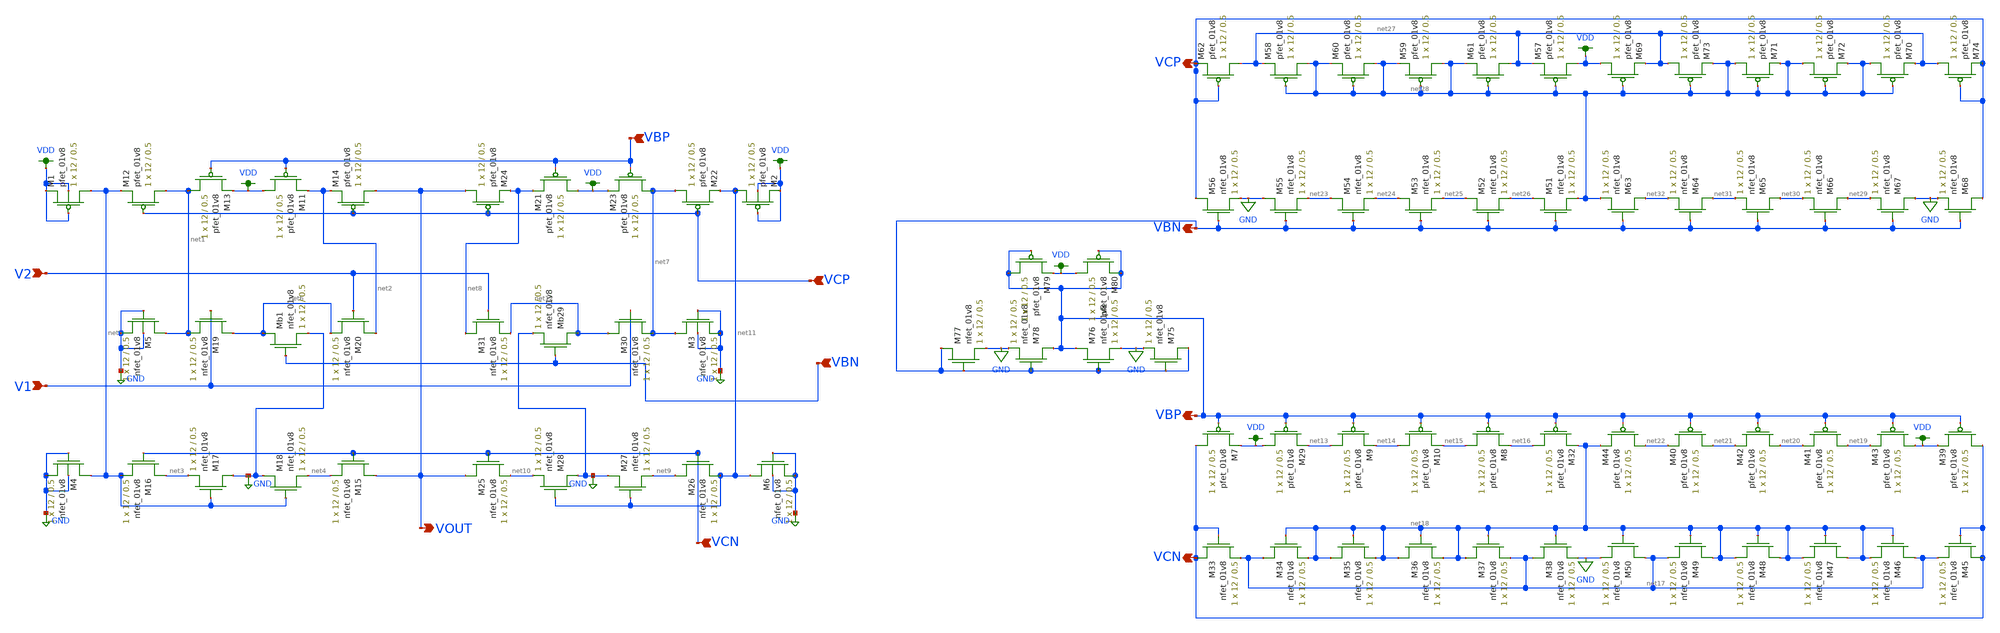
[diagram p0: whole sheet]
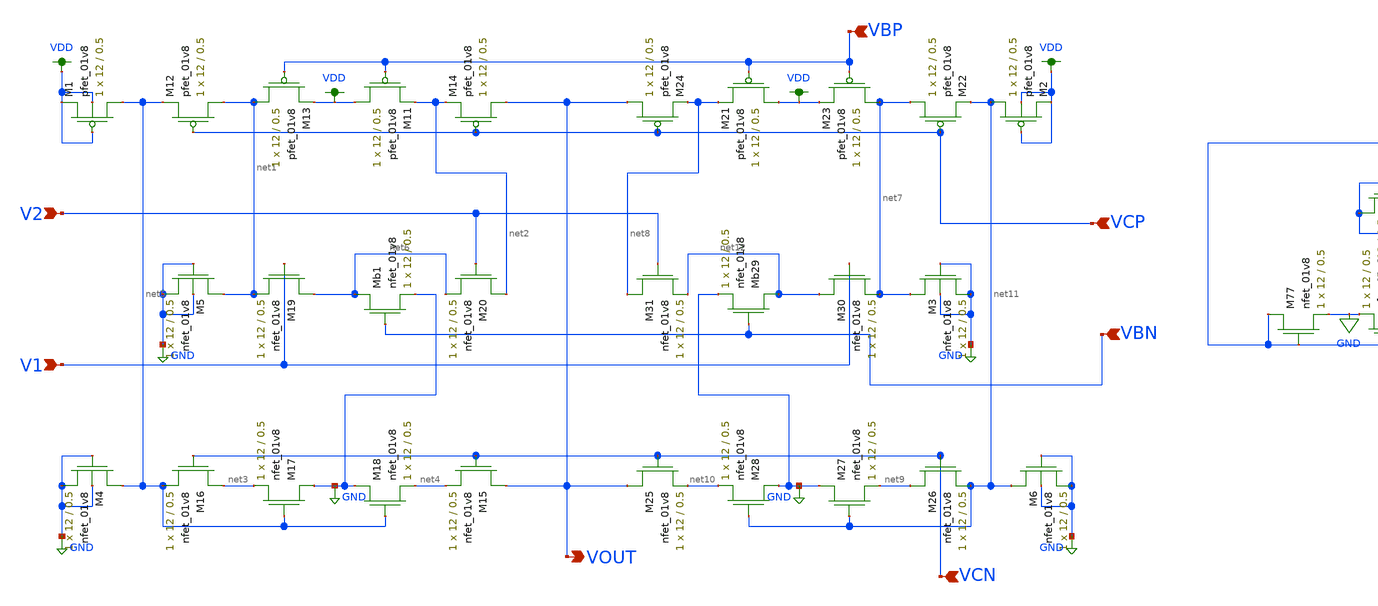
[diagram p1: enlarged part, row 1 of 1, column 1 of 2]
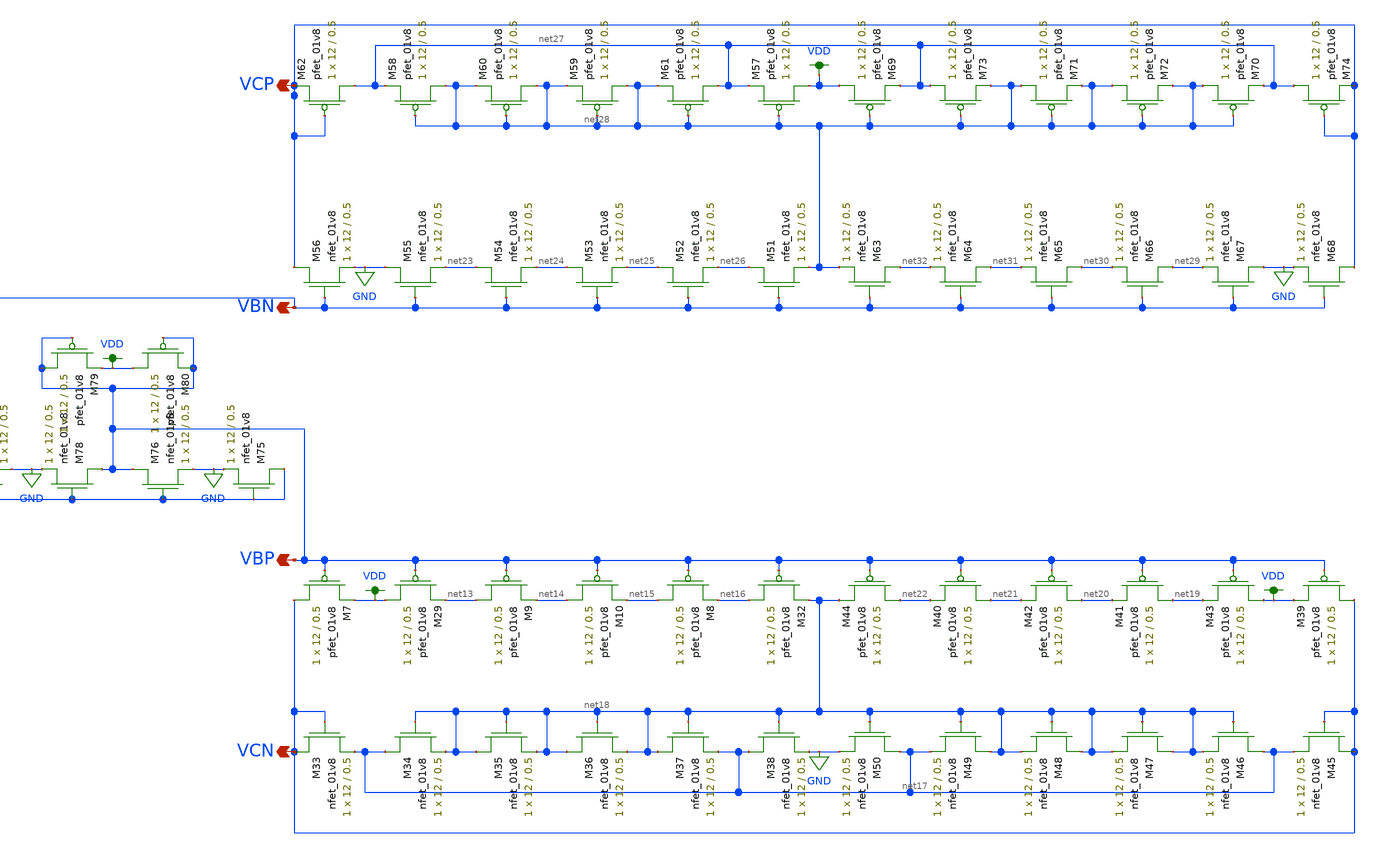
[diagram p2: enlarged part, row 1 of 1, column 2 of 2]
** sch_path: MP3/LVS/LVS_Circuit.sch
**.subckt LVS_Circuit VBP VCN VCP VOUT VBN V2 V1 VBP VCN VCP VBN
*.ipin VBP
*.ipin VCN
*.ipin VCP
*.opin VOUT
*.ipin VBN
*.ipin V2
*.ipin V1
*.opin VBP
*.opin VCN
*.opin VCP
*.opin VBN
XM11 VDD VBP net2 VDD sky130_fd_pr__pfet_01v8 L=0.5 W=12 nf=1 ad='int((nf+1)/2) * W/nf * 0.29' as='int((nf+2)/2) * W/nf * 0.29'
+ pd='2*int((nf+1)/2) * (W/nf + 0.29)' ps='2*int((nf+2)/2) * (W/nf + 0.29)' nrd='0.29 / W' nrs='0.29 / W'
+ sa=0 sb=0 sd=0 mult=1 m=1
XM12 net1 VCP net5 VDD sky130_fd_pr__pfet_01v8 L=0.5 W=12 nf=1 ad='int((nf+1)/2) * W/nf * 0.29' as='int((nf+2)/2) * W/nf * 0.29'
+ pd='2*int((nf+1)/2) * (W/nf + 0.29)' ps='2*int((nf+2)/2) * (W/nf + 0.29)' nrd='0.29 / W' nrs='0.29 / W'
+ sa=0 sb=0 sd=0 mult=1 m=1
XM13 net1 VBP VDD VDD sky130_fd_pr__pfet_01v8 L=0.5 W=12 nf=1 ad='int((nf+1)/2) * W/nf * 0.29' as='int((nf+2)/2) * W/nf * 0.29'
+ pd='2*int((nf+1)/2) * (W/nf + 0.29)' ps='2*int((nf+2)/2) * (W/nf + 0.29)' nrd='0.29 / W' nrs='0.29 / W'
+ sa=0 sb=0 sd=0 mult=1 m=1
XM14 VOUT VCP net2 VDD sky130_fd_pr__pfet_01v8 L=0.5 W=12 nf=1 ad='int((nf+1)/2) * W/nf * 0.29' as='int((nf+2)/2) * W/nf * 0.29'
+ pd='2*int((nf+1)/2) * (W/nf + 0.29)' ps='2*int((nf+2)/2) * (W/nf + 0.29)' nrd='0.29 / W' nrs='0.29 / W'
+ sa=0 sb=0 sd=0 mult=1 m=1
XM15 VOUT VCN net4 GND sky130_fd_pr__nfet_01v8 L=0.5 W=12 nf=1 ad='int((nf+1)/2) * W/nf * 0.29' as='int((nf+2)/2) * W/nf * 0.29'
+ pd='2*int((nf+1)/2) * (W/nf + 0.29)' ps='2*int((nf+2)/2) * (W/nf + 0.29)' nrd='0.29 / W' nrs='0.29 / W'
+ sa=0 sb=0 sd=0 mult=1 m=1
XM16 net3 VCN net5 GND sky130_fd_pr__nfet_01v8 L=0.5 W=12 nf=1 ad='int((nf+1)/2) * W/nf * 0.29' as='int((nf+2)/2) * W/nf * 0.29'
+ pd='2*int((nf+1)/2) * (W/nf + 0.29)' ps='2*int((nf+2)/2) * (W/nf + 0.29)' nrd='0.29 / W' nrs='0.29 / W'
+ sa=0 sb=0 sd=0 mult=1 m=1
XM17 GND net5 net3 GND sky130_fd_pr__nfet_01v8 L=0.5 W=12 nf=1 ad='int((nf+1)/2) * W/nf * 0.29' as='int((nf+2)/2) * W/nf * 0.29'
+ pd='2*int((nf+1)/2) * (W/nf + 0.29)' ps='2*int((nf+2)/2) * (W/nf + 0.29)' nrd='0.29 / W' nrs='0.29 / W'
+ sa=0 sb=0 sd=0 mult=1 m=1
XM18 GND net5 net4 GND sky130_fd_pr__nfet_01v8 L=0.5 W=12 nf=1 ad='int((nf+1)/2) * W/nf * 0.29' as='int((nf+2)/2) * W/nf * 0.29'
+ pd='2*int((nf+1)/2) * (W/nf + 0.29)' ps='2*int((nf+2)/2) * (W/nf + 0.29)' nrd='0.29 / W' nrs='0.29 / W'
+ sa=0 sb=0 sd=0 mult=1 m=1
XMb1 net6 VBN GND GND sky130_fd_pr__nfet_01v8 L=0.5 W=12 nf=1 ad='int((nf+1)/2) * W/nf * 0.29' as='int((nf+2)/2) * W/nf * 0.29'
+ pd='2*int((nf+1)/2) * (W/nf + 0.29)' ps='2*int((nf+2)/2) * (W/nf + 0.29)' nrd='0.29 / W' nrs='0.29 / W'
+ sa=0 sb=0 sd=0 mult=1 m=1
XM19 net6 V1 net1 GND sky130_fd_pr__nfet_01v8 L=0.5 W=12 nf=1 ad='int((nf+1)/2) * W/nf * 0.29' as='int((nf+2)/2) * W/nf * 0.29'
+ pd='2*int((nf+1)/2) * (W/nf + 0.29)' ps='2*int((nf+2)/2) * (W/nf + 0.29)' nrd='0.29 / W' nrs='0.29 / W'
+ sa=0 sb=0 sd=0 mult=1 m=1
XM20 net2 V2 net6 GND sky130_fd_pr__nfet_01v8 L=0.5 W=12 nf=1 ad='int((nf+1)/2) * W/nf * 0.29' as='int((nf+2)/2) * W/nf * 0.29'
+ pd='2*int((nf+1)/2) * (W/nf + 0.29)' ps='2*int((nf+2)/2) * (W/nf + 0.29)' nrd='0.29 / W' nrs='0.29 / W'
+ sa=0 sb=0 sd=0 mult=1 m=1
XM21 VDD VBP net8 VDD sky130_fd_pr__pfet_01v8 L=0.5 W=12 nf=1 ad='int((nf+1)/2) * W/nf * 0.29' as='int((nf+2)/2) * W/nf * 0.29'
+ pd='2*int((nf+1)/2) * (W/nf + 0.29)' ps='2*int((nf+2)/2) * (W/nf + 0.29)' nrd='0.29 / W' nrs='0.29 / W'
+ sa=0 sb=0 sd=0 mult=1 m=1
XM22 net7 VCP net11 VDD sky130_fd_pr__pfet_01v8 L=0.5 W=12 nf=1 ad='int((nf+1)/2) * W/nf * 0.29' as='int((nf+2)/2) * W/nf * 0.29'
+ pd='2*int((nf+1)/2) * (W/nf + 0.29)' ps='2*int((nf+2)/2) * (W/nf + 0.29)' nrd='0.29 / W' nrs='0.29 / W'
+ sa=0 sb=0 sd=0 mult=1 m=1
XM23 net7 VBP VDD VDD sky130_fd_pr__pfet_01v8 L=0.5 W=12 nf=1 ad='int((nf+1)/2) * W/nf * 0.29' as='int((nf+2)/2) * W/nf * 0.29'
+ pd='2*int((nf+1)/2) * (W/nf + 0.29)' ps='2*int((nf+2)/2) * (W/nf + 0.29)' nrd='0.29 / W' nrs='0.29 / W'
+ sa=0 sb=0 sd=0 mult=1 m=1
XM24 VOUT VCP net8 VDD sky130_fd_pr__pfet_01v8 L=0.5 W=12 nf=1 ad='int((nf+1)/2) * W/nf * 0.29' as='int((nf+2)/2) * W/nf * 0.29'
+ pd='2*int((nf+1)/2) * (W/nf + 0.29)' ps='2*int((nf+2)/2) * (W/nf + 0.29)' nrd='0.29 / W' nrs='0.29 / W'
+ sa=0 sb=0 sd=0 mult=1 m=1
XM25 VOUT VCN net10 GND sky130_fd_pr__nfet_01v8 L=0.5 W=12 nf=1 ad='int((nf+1)/2) * W/nf * 0.29' as='int((nf+2)/2) * W/nf * 0.29'
+ pd='2*int((nf+1)/2) * (W/nf + 0.29)' ps='2*int((nf+2)/2) * (W/nf + 0.29)' nrd='0.29 / W' nrs='0.29 / W'
+ sa=0 sb=0 sd=0 mult=1 m=1
XM26 net9 VCN net11 GND sky130_fd_pr__nfet_01v8 L=0.5 W=12 nf=1 ad='int((nf+1)/2) * W/nf * 0.29' as='int((nf+2)/2) * W/nf * 0.29'
+ pd='2*int((nf+1)/2) * (W/nf + 0.29)' ps='2*int((nf+2)/2) * (W/nf + 0.29)' nrd='0.29 / W' nrs='0.29 / W'
+ sa=0 sb=0 sd=0 mult=1 m=1
XM27 GND net11 net9 GND sky130_fd_pr__nfet_01v8 L=0.5 W=12 nf=1 ad='int((nf+1)/2) * W/nf * 0.29' as='int((nf+2)/2) * W/nf * 0.29'
+ pd='2*int((nf+1)/2) * (W/nf + 0.29)' ps='2*int((nf+2)/2) * (W/nf + 0.29)' nrd='0.29 / W' nrs='0.29 / W'
+ sa=0 sb=0 sd=0 mult=1 m=1
XM28 GND net11 net10 GND sky130_fd_pr__nfet_01v8 L=0.5 W=12 nf=1 ad='int((nf+1)/2) * W/nf * 0.29' as='int((nf+2)/2) * W/nf * 0.29'
+ pd='2*int((nf+1)/2) * (W/nf + 0.29)' ps='2*int((nf+2)/2) * (W/nf + 0.29)' nrd='0.29 / W' nrs='0.29 / W'
+ sa=0 sb=0 sd=0 mult=1 m=1
XMb29 net12 VBN GND GND sky130_fd_pr__nfet_01v8 L=0.5 W=12 nf=1 ad='int((nf+1)/2) * W/nf * 0.29' as='int((nf+2)/2) * W/nf * 0.29'
+ pd='2*int((nf+1)/2) * (W/nf + 0.29)' ps='2*int((nf+2)/2) * (W/nf + 0.29)' nrd='0.29 / W' nrs='0.29 / W'
+ sa=0 sb=0 sd=0 mult=1 m=1
XM30 net12 V1 net7 GND sky130_fd_pr__nfet_01v8 L=0.5 W=12 nf=1 ad='int((nf+1)/2) * W/nf * 0.29' as='int((nf+2)/2) * W/nf * 0.29'
+ pd='2*int((nf+1)/2) * (W/nf + 0.29)' ps='2*int((nf+2)/2) * (W/nf + 0.29)' nrd='0.29 / W' nrs='0.29 / W'
+ sa=0 sb=0 sd=0 mult=1 m=1
XM31 net8 V2 net12 GND sky130_fd_pr__nfet_01v8 L=0.5 W=12 nf=1 ad='int((nf+1)/2) * W/nf * 0.29' as='int((nf+2)/2) * W/nf * 0.29'
+ pd='2*int((nf+1)/2) * (W/nf + 0.29)' ps='2*int((nf+2)/2) * (W/nf + 0.29)' nrd='0.29 / W' nrs='0.29 / W'
+ sa=0 sb=0 sd=0 mult=1 m=1
XM1 net5 VDD VDD VDD sky130_fd_pr__pfet_01v8 L=0.5 W=12 nf=1 ad='int((nf+1)/2) * W/nf * 0.29' as='int((nf+2)/2) * W/nf * 0.29'
+ pd='2*int((nf+1)/2) * (W/nf + 0.29)' ps='2*int((nf+2)/2) * (W/nf + 0.29)' nrd='0.29 / W' nrs='0.29 / W'
+ sa=0 sb=0 sd=0 mult=1 m=1
XM2 net11 VDD VDD VDD sky130_fd_pr__pfet_01v8 L=0.5 W=12 nf=1 ad='int((nf+1)/2) * W/nf * 0.29' as='int((nf+2)/2) * W/nf * 0.29'
+ pd='2*int((nf+1)/2) * (W/nf + 0.29)' ps='2*int((nf+2)/2) * (W/nf + 0.29)' nrd='0.29 / W' nrs='0.29 / W'
+ sa=0 sb=0 sd=0 mult=1 m=1
XM4 net5 GND GND GND sky130_fd_pr__nfet_01v8 L=0.5 W=12 nf=1 ad='int((nf+1)/2) * W/nf * 0.29' as='int((nf+2)/2) * W/nf * 0.29'
+ pd='2*int((nf+1)/2) * (W/nf + 0.29)' ps='2*int((nf+2)/2) * (W/nf + 0.29)' nrd='0.29 / W' nrs='0.29 / W'
+ sa=0 sb=0 sd=0 mult=1 m=1
XM3 net7 GND GND GND sky130_fd_pr__nfet_01v8 L=0.5 W=12 nf=1 ad='int((nf+1)/2) * W/nf * 0.29' as='int((nf+2)/2) * W/nf * 0.29'
+ pd='2*int((nf+1)/2) * (W/nf + 0.29)' ps='2*int((nf+2)/2) * (W/nf + 0.29)' nrd='0.29 / W' nrs='0.29 / W'
+ sa=0 sb=0 sd=0 mult=1 m=1
XM5 net1 GND GND GND sky130_fd_pr__nfet_01v8 L=0.5 W=12 nf=1 ad='int((nf+1)/2) * W/nf * 0.29' as='int((nf+2)/2) * W/nf * 0.29'
+ pd='2*int((nf+1)/2) * (W/nf + 0.29)' ps='2*int((nf+2)/2) * (W/nf + 0.29)' nrd='0.29 / W' nrs='0.29 / W'
+ sa=0 sb=0 sd=0 mult=1 m=1
XM6 net11 GND GND GND sky130_fd_pr__nfet_01v8 L=0.5 W=12 nf=1 ad='int((nf+1)/2) * W/nf * 0.29' as='int((nf+2)/2) * W/nf * 0.29'
+ pd='2*int((nf+1)/2) * (W/nf + 0.29)' ps='2*int((nf+2)/2) * (W/nf + 0.29)' nrd='0.29 / W' nrs='0.29 / W'
+ sa=0 sb=0 sd=0 mult=1 m=1
XM7 VCN VBP VDD VDD sky130_fd_pr__pfet_01v8 L=0.5 W=12 nf=1 ad='int((nf+1)/2) * W/nf * 0.29' as='int((nf+2)/2) * W/nf * 0.29'
+ pd='2*int((nf+1)/2) * (W/nf + 0.29)' ps='2*int((nf+2)/2) * (W/nf + 0.29)' nrd='0.29 / W' nrs='0.29 / W'
+ sa=0 sb=0 sd=0 mult=1 m=1
XM8 net15 VBP net16 VDD sky130_fd_pr__pfet_01v8 L=0.5 W=12 nf=1 ad='int((nf+1)/2) * W/nf * 0.29' as='int((nf+2)/2) * W/nf * 0.29'
+ pd='2*int((nf+1)/2) * (W/nf + 0.29)' ps='2*int((nf+2)/2) * (W/nf + 0.29)' nrd='0.29 / W' nrs='0.29 / W'
+ sa=0 sb=0 sd=0 mult=1 m=1
XM9 net13 VBP net14 VDD sky130_fd_pr__pfet_01v8 L=0.5 W=12 nf=1 ad='int((nf+1)/2) * W/nf * 0.29' as='int((nf+2)/2) * W/nf * 0.29'
+ pd='2*int((nf+1)/2) * (W/nf + 0.29)' ps='2*int((nf+2)/2) * (W/nf + 0.29)' nrd='0.29 / W' nrs='0.29 / W'
+ sa=0 sb=0 sd=0 mult=1 m=1
XM10 net14 VBP net15 VDD sky130_fd_pr__pfet_01v8 L=0.5 W=12 nf=1 ad='int((nf+1)/2) * W/nf * 0.29' as='int((nf+2)/2) * W/nf * 0.29'
+ pd='2*int((nf+1)/2) * (W/nf + 0.29)' ps='2*int((nf+2)/2) * (W/nf + 0.29)' nrd='0.29 / W' nrs='0.29 / W'
+ sa=0 sb=0 sd=0 mult=1 m=1
XM29 VDD VBP net13 VDD sky130_fd_pr__pfet_01v8 L=0.5 W=12 nf=1 ad='int((nf+1)/2) * W/nf * 0.29' as='int((nf+2)/2) * W/nf * 0.29'
+ pd='2*int((nf+1)/2) * (W/nf + 0.29)' ps='2*int((nf+2)/2) * (W/nf + 0.29)' nrd='0.29 / W' nrs='0.29 / W'
+ sa=0 sb=0 sd=0 mult=1 m=1
XM32 net16 VBP net18 VDD sky130_fd_pr__pfet_01v8 L=0.5 W=12 nf=1 ad='int((nf+1)/2) * W/nf * 0.29' as='int((nf+2)/2) * W/nf * 0.29'
+ pd='2*int((nf+1)/2) * (W/nf + 0.29)' ps='2*int((nf+2)/2) * (W/nf + 0.29)' nrd='0.29 / W' nrs='0.29 / W'
+ sa=0 sb=0 sd=0 mult=1 m=1
XM33 VCN VCN net17 GND sky130_fd_pr__nfet_01v8 L=0.5 W=12 nf=1 ad='int((nf+1)/2) * W/nf * 0.29' as='int((nf+2)/2) * W/nf * 0.29'
+ pd='2*int((nf+1)/2) * (W/nf + 0.29)' ps='2*int((nf+2)/2) * (W/nf + 0.29)' nrd='0.29 / W' nrs='0.29 / W'
+ sa=0 sb=0 sd=0 mult=1 m=1
XM34 net17 net18 net18 GND sky130_fd_pr__nfet_01v8 L=0.5 W=12 nf=1 ad='int((nf+1)/2) * W/nf * 0.29' as='int((nf+2)/2) * W/nf * 0.29'
+ pd='2*int((nf+1)/2) * (W/nf + 0.29)' ps='2*int((nf+2)/2) * (W/nf + 0.29)' nrd='0.29 / W' nrs='0.29 / W'
+ sa=0 sb=0 sd=0 mult=1 m=1
XM35 net18 net18 net18 GND sky130_fd_pr__nfet_01v8 L=0.5 W=12 nf=1 ad='int((nf+1)/2) * W/nf * 0.29' as='int((nf+2)/2) * W/nf * 0.29'
+ pd='2*int((nf+1)/2) * (W/nf + 0.29)' ps='2*int((nf+2)/2) * (W/nf + 0.29)' nrd='0.29 / W' nrs='0.29 / W'
+ sa=0 sb=0 sd=0 mult=1 m=1
XM36 net18 net18 net18 GND sky130_fd_pr__nfet_01v8 L=0.5 W=12 nf=1 ad='int((nf+1)/2) * W/nf * 0.29' as='int((nf+2)/2) * W/nf * 0.29'
+ pd='2*int((nf+1)/2) * (W/nf + 0.29)' ps='2*int((nf+2)/2) * (W/nf + 0.29)' nrd='0.29 / W' nrs='0.29 / W'
+ sa=0 sb=0 sd=0 mult=1 m=1
XM37 net18 net18 net17 GND sky130_fd_pr__nfet_01v8 L=0.5 W=12 nf=1 ad='int((nf+1)/2) * W/nf * 0.29' as='int((nf+2)/2) * W/nf * 0.29'
+ pd='2*int((nf+1)/2) * (W/nf + 0.29)' ps='2*int((nf+2)/2) * (W/nf + 0.29)' nrd='0.29 / W' nrs='0.29 / W'
+ sa=0 sb=0 sd=0 mult=1 m=1
XM38 net17 net18 GND GND sky130_fd_pr__nfet_01v8 L=0.5 W=12 nf=1 ad='int((nf+1)/2) * W/nf * 0.29' as='int((nf+2)/2) * W/nf * 0.29'
+ pd='2*int((nf+1)/2) * (W/nf + 0.29)' ps='2*int((nf+2)/2) * (W/nf + 0.29)' nrd='0.29 / W' nrs='0.29 / W'
+ sa=0 sb=0 sd=0 mult=1 m=1
XM39 VCN VBP VDD VDD sky130_fd_pr__pfet_01v8 L=0.5 W=12 nf=1 ad='int((nf+1)/2) * W/nf * 0.29' as='int((nf+2)/2) * W/nf * 0.29'
+ pd='2*int((nf+1)/2) * (W/nf + 0.29)' ps='2*int((nf+2)/2) * (W/nf + 0.29)' nrd='0.29 / W' nrs='0.29 / W'
+ sa=0 sb=0 sd=0 mult=1 m=1
XM40 net21 VBP net22 VDD sky130_fd_pr__pfet_01v8 L=0.5 W=12 nf=1 ad='int((nf+1)/2) * W/nf * 0.29' as='int((nf+2)/2) * W/nf * 0.29'
+ pd='2*int((nf+1)/2) * (W/nf + 0.29)' ps='2*int((nf+2)/2) * (W/nf + 0.29)' nrd='0.29 / W' nrs='0.29 / W'
+ sa=0 sb=0 sd=0 mult=1 m=1
XM41 net19 VBP net20 VDD sky130_fd_pr__pfet_01v8 L=0.5 W=12 nf=1 ad='int((nf+1)/2) * W/nf * 0.29' as='int((nf+2)/2) * W/nf * 0.29'
+ pd='2*int((nf+1)/2) * (W/nf + 0.29)' ps='2*int((nf+2)/2) * (W/nf + 0.29)' nrd='0.29 / W' nrs='0.29 / W'
+ sa=0 sb=0 sd=0 mult=1 m=1
XM42 net20 VBP net21 VDD sky130_fd_pr__pfet_01v8 L=0.5 W=12 nf=1 ad='int((nf+1)/2) * W/nf * 0.29' as='int((nf+2)/2) * W/nf * 0.29'
+ pd='2*int((nf+1)/2) * (W/nf + 0.29)' ps='2*int((nf+2)/2) * (W/nf + 0.29)' nrd='0.29 / W' nrs='0.29 / W'
+ sa=0 sb=0 sd=0 mult=1 m=1
XM43 VDD VBP net19 VDD sky130_fd_pr__pfet_01v8 L=0.5 W=12 nf=1 ad='int((nf+1)/2) * W/nf * 0.29' as='int((nf+2)/2) * W/nf * 0.29'
+ pd='2*int((nf+1)/2) * (W/nf + 0.29)' ps='2*int((nf+2)/2) * (W/nf + 0.29)' nrd='0.29 / W' nrs='0.29 / W'
+ sa=0 sb=0 sd=0 mult=1 m=1
XM44 net22 VBP net18 VDD sky130_fd_pr__pfet_01v8 L=0.5 W=12 nf=1 ad='int((nf+1)/2) * W/nf * 0.29' as='int((nf+2)/2) * W/nf * 0.29'
+ pd='2*int((nf+1)/2) * (W/nf + 0.29)' ps='2*int((nf+2)/2) * (W/nf + 0.29)' nrd='0.29 / W' nrs='0.29 / W'
+ sa=0 sb=0 sd=0 mult=1 m=1
XM45 VCN VCN net17 GND sky130_fd_pr__nfet_01v8 L=0.5 W=12 nf=1 ad='int((nf+1)/2) * W/nf * 0.29' as='int((nf+2)/2) * W/nf * 0.29'
+ pd='2*int((nf+1)/2) * (W/nf + 0.29)' ps='2*int((nf+2)/2) * (W/nf + 0.29)' nrd='0.29 / W' nrs='0.29 / W'
+ sa=0 sb=0 sd=0 mult=1 m=1
XM46 net17 net18 net18 GND sky130_fd_pr__nfet_01v8 L=0.5 W=12 nf=1 ad='int((nf+1)/2) * W/nf * 0.29' as='int((nf+2)/2) * W/nf * 0.29'
+ pd='2*int((nf+1)/2) * (W/nf + 0.29)' ps='2*int((nf+2)/2) * (W/nf + 0.29)' nrd='0.29 / W' nrs='0.29 / W'
+ sa=0 sb=0 sd=0 mult=1 m=1
XM47 net18 net18 net18 GND sky130_fd_pr__nfet_01v8 L=0.5 W=12 nf=1 ad='int((nf+1)/2) * W/nf * 0.29' as='int((nf+2)/2) * W/nf * 0.29'
+ pd='2*int((nf+1)/2) * (W/nf + 0.29)' ps='2*int((nf+2)/2) * (W/nf + 0.29)' nrd='0.29 / W' nrs='0.29 / W'
+ sa=0 sb=0 sd=0 mult=1 m=1
XM48 net18 net18 net18 GND sky130_fd_pr__nfet_01v8 L=0.5 W=12 nf=1 ad='int((nf+1)/2) * W/nf * 0.29' as='int((nf+2)/2) * W/nf * 0.29'
+ pd='2*int((nf+1)/2) * (W/nf + 0.29)' ps='2*int((nf+2)/2) * (W/nf + 0.29)' nrd='0.29 / W' nrs='0.29 / W'
+ sa=0 sb=0 sd=0 mult=1 m=1
XM49 net18 net18 net17 GND sky130_fd_pr__nfet_01v8 L=0.5 W=12 nf=1 ad='int((nf+1)/2) * W/nf * 0.29' as='int((nf+2)/2) * W/nf * 0.29'
+ pd='2*int((nf+1)/2) * (W/nf + 0.29)' ps='2*int((nf+2)/2) * (W/nf + 0.29)' nrd='0.29 / W' nrs='0.29 / W'
+ sa=0 sb=0 sd=0 mult=1 m=1
XM50 net17 net18 GND GND sky130_fd_pr__nfet_01v8 L=0.5 W=12 nf=1 ad='int((nf+1)/2) * W/nf * 0.29' as='int((nf+2)/2) * W/nf * 0.29'
+ pd='2*int((nf+1)/2) * (W/nf + 0.29)' ps='2*int((nf+2)/2) * (W/nf + 0.29)' nrd='0.29 / W' nrs='0.29 / W'
+ sa=0 sb=0 sd=0 mult=1 m=1
XM51 net26 VBN net28 GND sky130_fd_pr__nfet_01v8 L=0.5 W=12 nf=1 ad='int((nf+1)/2) * W/nf * 0.29' as='int((nf+2)/2) * W/nf * 0.29'
+ pd='2*int((nf+1)/2) * (W/nf + 0.29)' ps='2*int((nf+2)/2) * (W/nf + 0.29)' nrd='0.29 / W' nrs='0.29 / W'
+ sa=0 sb=0 sd=0 mult=1 m=1
XM52 net25 VBN net26 GND sky130_fd_pr__nfet_01v8 L=0.5 W=12 nf=1 ad='int((nf+1)/2) * W/nf * 0.29' as='int((nf+2)/2) * W/nf * 0.29'
+ pd='2*int((nf+1)/2) * (W/nf + 0.29)' ps='2*int((nf+2)/2) * (W/nf + 0.29)' nrd='0.29 / W' nrs='0.29 / W'
+ sa=0 sb=0 sd=0 mult=1 m=1
XM53 net24 VBN net25 GND sky130_fd_pr__nfet_01v8 L=0.5 W=12 nf=1 ad='int((nf+1)/2) * W/nf * 0.29' as='int((nf+2)/2) * W/nf * 0.29'
+ pd='2*int((nf+1)/2) * (W/nf + 0.29)' ps='2*int((nf+2)/2) * (W/nf + 0.29)' nrd='0.29 / W' nrs='0.29 / W'
+ sa=0 sb=0 sd=0 mult=1 m=1
XM54 net23 VBN net24 GND sky130_fd_pr__nfet_01v8 L=0.5 W=12 nf=1 ad='int((nf+1)/2) * W/nf * 0.29' as='int((nf+2)/2) * W/nf * 0.29'
+ pd='2*int((nf+1)/2) * (W/nf + 0.29)' ps='2*int((nf+2)/2) * (W/nf + 0.29)' nrd='0.29 / W' nrs='0.29 / W'
+ sa=0 sb=0 sd=0 mult=1 m=1
XM55 GND VBN net23 GND sky130_fd_pr__nfet_01v8 L=0.5 W=12 nf=1 ad='int((nf+1)/2) * W/nf * 0.29' as='int((nf+2)/2) * W/nf * 0.29'
+ pd='2*int((nf+1)/2) * (W/nf + 0.29)' ps='2*int((nf+2)/2) * (W/nf + 0.29)' nrd='0.29 / W' nrs='0.29 / W'
+ sa=0 sb=0 sd=0 mult=1 m=1
XM56 VCP VBN GND GND sky130_fd_pr__nfet_01v8 L=0.5 W=12 nf=1 ad='int((nf+1)/2) * W/nf * 0.29' as='int((nf+2)/2) * W/nf * 0.29'
+ pd='2*int((nf+1)/2) * (W/nf + 0.29)' ps='2*int((nf+2)/2) * (W/nf + 0.29)' nrd='0.29 / W' nrs='0.29 / W'
+ sa=0 sb=0 sd=0 mult=1 m=1
XM57 VDD net28 net27 VDD sky130_fd_pr__pfet_01v8 L=0.5 W=12 nf=1 ad='int((nf+1)/2) * W/nf * 0.29' as='int((nf+2)/2) * W/nf * 0.29'
+ pd='2*int((nf+1)/2) * (W/nf + 0.29)' ps='2*int((nf+2)/2) * (W/nf + 0.29)' nrd='0.29 / W' nrs='0.29 / W'
+ sa=0 sb=0 sd=0 mult=1 m=1
XM58 net28 net28 net27 VDD sky130_fd_pr__pfet_01v8 L=0.5 W=12 nf=1 ad='int((nf+1)/2) * W/nf * 0.29' as='int((nf+2)/2) * W/nf * 0.29'
+ pd='2*int((nf+1)/2) * (W/nf + 0.29)' ps='2*int((nf+2)/2) * (W/nf + 0.29)' nrd='0.29 / W' nrs='0.29 / W'
+ sa=0 sb=0 sd=0 mult=1 m=1
XM59 net28 net28 net28 VDD sky130_fd_pr__pfet_01v8 L=0.5 W=12 nf=1 ad='int((nf+1)/2) * W/nf * 0.29' as='int((nf+2)/2) * W/nf * 0.29'
+ pd='2*int((nf+1)/2) * (W/nf + 0.29)' ps='2*int((nf+2)/2) * (W/nf + 0.29)' nrd='0.29 / W' nrs='0.29 / W'
+ sa=0 sb=0 sd=0 mult=1 m=1
XM60 net28 net28 net28 VDD sky130_fd_pr__pfet_01v8 L=0.5 W=12 nf=1 ad='int((nf+1)/2) * W/nf * 0.29' as='int((nf+2)/2) * W/nf * 0.29'
+ pd='2*int((nf+1)/2) * (W/nf + 0.29)' ps='2*int((nf+2)/2) * (W/nf + 0.29)' nrd='0.29 / W' nrs='0.29 / W'
+ sa=0 sb=0 sd=0 mult=1 m=1
XM61 net27 net28 net28 VDD sky130_fd_pr__pfet_01v8 L=0.5 W=12 nf=1 ad='int((nf+1)/2) * W/nf * 0.29' as='int((nf+2)/2) * W/nf * 0.29'
+ pd='2*int((nf+1)/2) * (W/nf + 0.29)' ps='2*int((nf+2)/2) * (W/nf + 0.29)' nrd='0.29 / W' nrs='0.29 / W'
+ sa=0 sb=0 sd=0 mult=1 m=1
XM62 net27 VCP VCP VDD sky130_fd_pr__pfet_01v8 L=0.5 W=12 nf=1 ad='int((nf+1)/2) * W/nf * 0.29' as='int((nf+2)/2) * W/nf * 0.29'
+ pd='2*int((nf+1)/2) * (W/nf + 0.29)' ps='2*int((nf+2)/2) * (W/nf + 0.29)' nrd='0.29 / W' nrs='0.29 / W'
+ sa=0 sb=0 sd=0 mult=1 m=1
XM63 net32 VBN net28 GND sky130_fd_pr__nfet_01v8 L=0.5 W=12 nf=1 ad='int((nf+1)/2) * W/nf * 0.29' as='int((nf+2)/2) * W/nf * 0.29'
+ pd='2*int((nf+1)/2) * (W/nf + 0.29)' ps='2*int((nf+2)/2) * (W/nf + 0.29)' nrd='0.29 / W' nrs='0.29 / W'
+ sa=0 sb=0 sd=0 mult=1 m=1
XM64 net31 VBN net32 GND sky130_fd_pr__nfet_01v8 L=0.5 W=12 nf=1 ad='int((nf+1)/2) * W/nf * 0.29' as='int((nf+2)/2) * W/nf * 0.29'
+ pd='2*int((nf+1)/2) * (W/nf + 0.29)' ps='2*int((nf+2)/2) * (W/nf + 0.29)' nrd='0.29 / W' nrs='0.29 / W'
+ sa=0 sb=0 sd=0 mult=1 m=1
XM65 net30 VBN net31 GND sky130_fd_pr__nfet_01v8 L=0.5 W=12 nf=1 ad='int((nf+1)/2) * W/nf * 0.29' as='int((nf+2)/2) * W/nf * 0.29'
+ pd='2*int((nf+1)/2) * (W/nf + 0.29)' ps='2*int((nf+2)/2) * (W/nf + 0.29)' nrd='0.29 / W' nrs='0.29 / W'
+ sa=0 sb=0 sd=0 mult=1 m=1
XM66 net29 VBN net30 GND sky130_fd_pr__nfet_01v8 L=0.5 W=12 nf=1 ad='int((nf+1)/2) * W/nf * 0.29' as='int((nf+2)/2) * W/nf * 0.29'
+ pd='2*int((nf+1)/2) * (W/nf + 0.29)' ps='2*int((nf+2)/2) * (W/nf + 0.29)' nrd='0.29 / W' nrs='0.29 / W'
+ sa=0 sb=0 sd=0 mult=1 m=1
XM67 GND VBN net29 GND sky130_fd_pr__nfet_01v8 L=0.5 W=12 nf=1 ad='int((nf+1)/2) * W/nf * 0.29' as='int((nf+2)/2) * W/nf * 0.29'
+ pd='2*int((nf+1)/2) * (W/nf + 0.29)' ps='2*int((nf+2)/2) * (W/nf + 0.29)' nrd='0.29 / W' nrs='0.29 / W'
+ sa=0 sb=0 sd=0 mult=1 m=1
XM68 VCP VBN GND GND sky130_fd_pr__nfet_01v8 L=0.5 W=12 nf=1 ad='int((nf+1)/2) * W/nf * 0.29' as='int((nf+2)/2) * W/nf * 0.29'
+ pd='2*int((nf+1)/2) * (W/nf + 0.29)' ps='2*int((nf+2)/2) * (W/nf + 0.29)' nrd='0.29 / W' nrs='0.29 / W'
+ sa=0 sb=0 sd=0 mult=1 m=1
XM69 VDD net28 net27 VDD sky130_fd_pr__pfet_01v8 L=0.5 W=12 nf=1 ad='int((nf+1)/2) * W/nf * 0.29' as='int((nf+2)/2) * W/nf * 0.29'
+ pd='2*int((nf+1)/2) * (W/nf + 0.29)' ps='2*int((nf+2)/2) * (W/nf + 0.29)' nrd='0.29 / W' nrs='0.29 / W'
+ sa=0 sb=0 sd=0 mult=1 m=1
XM70 net28 net28 net27 VDD sky130_fd_pr__pfet_01v8 L=0.5 W=12 nf=1 ad='int((nf+1)/2) * W/nf * 0.29' as='int((nf+2)/2) * W/nf * 0.29'
+ pd='2*int((nf+1)/2) * (W/nf + 0.29)' ps='2*int((nf+2)/2) * (W/nf + 0.29)' nrd='0.29 / W' nrs='0.29 / W'
+ sa=0 sb=0 sd=0 mult=1 m=1
XM71 net28 net28 net28 VDD sky130_fd_pr__pfet_01v8 L=0.5 W=12 nf=1 ad='int((nf+1)/2) * W/nf * 0.29' as='int((nf+2)/2) * W/nf * 0.29'
+ pd='2*int((nf+1)/2) * (W/nf + 0.29)' ps='2*int((nf+2)/2) * (W/nf + 0.29)' nrd='0.29 / W' nrs='0.29 / W'
+ sa=0 sb=0 sd=0 mult=1 m=1
XM72 net28 net28 net28 VDD sky130_fd_pr__pfet_01v8 L=0.5 W=12 nf=1 ad='int((nf+1)/2) * W/nf * 0.29' as='int((nf+2)/2) * W/nf * 0.29'
+ pd='2*int((nf+1)/2) * (W/nf + 0.29)' ps='2*int((nf+2)/2) * (W/nf + 0.29)' nrd='0.29 / W' nrs='0.29 / W'
+ sa=0 sb=0 sd=0 mult=1 m=1
XM73 net27 net28 net28 VDD sky130_fd_pr__pfet_01v8 L=0.5 W=12 nf=1 ad='int((nf+1)/2) * W/nf * 0.29' as='int((nf+2)/2) * W/nf * 0.29'
+ pd='2*int((nf+1)/2) * (W/nf + 0.29)' ps='2*int((nf+2)/2) * (W/nf + 0.29)' nrd='0.29 / W' nrs='0.29 / W'
+ sa=0 sb=0 sd=0 mult=1 m=1
XM74 net27 VCP VCP VDD sky130_fd_pr__pfet_01v8 L=0.5 W=12 nf=1 ad='int((nf+1)/2) * W/nf * 0.29' as='int((nf+2)/2) * W/nf * 0.29'
+ pd='2*int((nf+1)/2) * (W/nf + 0.29)' ps='2*int((nf+2)/2) * (W/nf + 0.29)' nrd='0.29 / W' nrs='0.29 / W'
+ sa=0 sb=0 sd=0 mult=1 m=1
XM75 VBN VBN GND GND sky130_fd_pr__nfet_01v8 L=0.5 W=12 nf=1 ad='int((nf+1)/2) * W/nf * 0.29' as='int((nf+2)/2) * W/nf * 0.29'
+ pd='2*int((nf+1)/2) * (W/nf + 0.29)' ps='2*int((nf+2)/2) * (W/nf + 0.29)' nrd='0.29 / W' nrs='0.29 / W'
+ sa=0 sb=0 sd=0 mult=1 m=1
XM76 VBP VBN GND GND sky130_fd_pr__nfet_01v8 L=0.5 W=12 nf=1 ad='int((nf+1)/2) * W/nf * 0.29' as='int((nf+2)/2) * W/nf * 0.29'
+ pd='2*int((nf+1)/2) * (W/nf + 0.29)' ps='2*int((nf+2)/2) * (W/nf + 0.29)' nrd='0.29 / W' nrs='0.29 / W'
+ sa=0 sb=0 sd=0 mult=1 m=1
XM77 VBN VBN GND GND sky130_fd_pr__nfet_01v8 L=0.5 W=12 nf=1 ad='int((nf+1)/2) * W/nf * 0.29' as='int((nf+2)/2) * W/nf * 0.29'
+ pd='2*int((nf+1)/2) * (W/nf + 0.29)' ps='2*int((nf+2)/2) * (W/nf + 0.29)' nrd='0.29 / W' nrs='0.29 / W'
+ sa=0 sb=0 sd=0 mult=1 m=1
XM78 VBP VBN GND GND sky130_fd_pr__nfet_01v8 L=0.5 W=12 nf=1 ad='int((nf+1)/2) * W/nf * 0.29' as='int((nf+2)/2) * W/nf * 0.29'
+ pd='2*int((nf+1)/2) * (W/nf + 0.29)' ps='2*int((nf+2)/2) * (W/nf + 0.29)' nrd='0.29 / W' nrs='0.29 / W'
+ sa=0 sb=0 sd=0 mult=1 m=1
XM79 VBP VBP VDD VDD sky130_fd_pr__pfet_01v8 L=0.5 W=12 nf=1 ad='int((nf+1)/2) * W/nf * 0.29' as='int((nf+2)/2) * W/nf * 0.29'
+ pd='2*int((nf+1)/2) * (W/nf + 0.29)' ps='2*int((nf+2)/2) * (W/nf + 0.29)' nrd='0.29 / W' nrs='0.29 / W'
+ sa=0 sb=0 sd=0 mult=1 m=1
XM80 VDD VBP VBP VDD sky130_fd_pr__pfet_01v8 L=0.5 W=12 nf=1 ad='int((nf+1)/2) * W/nf * 0.29' as='int((nf+2)/2) * W/nf * 0.29'
+ pd='2*int((nf+1)/2) * (W/nf + 0.29)' ps='2*int((nf+2)/2) * (W/nf + 0.29)' nrd='0.29 / W' nrs='0.29 / W'
+ sa=0 sb=0 sd=0 mult=1 m=1
**.ends
.GLOBAL VDD
.GLOBAL GND
.end
